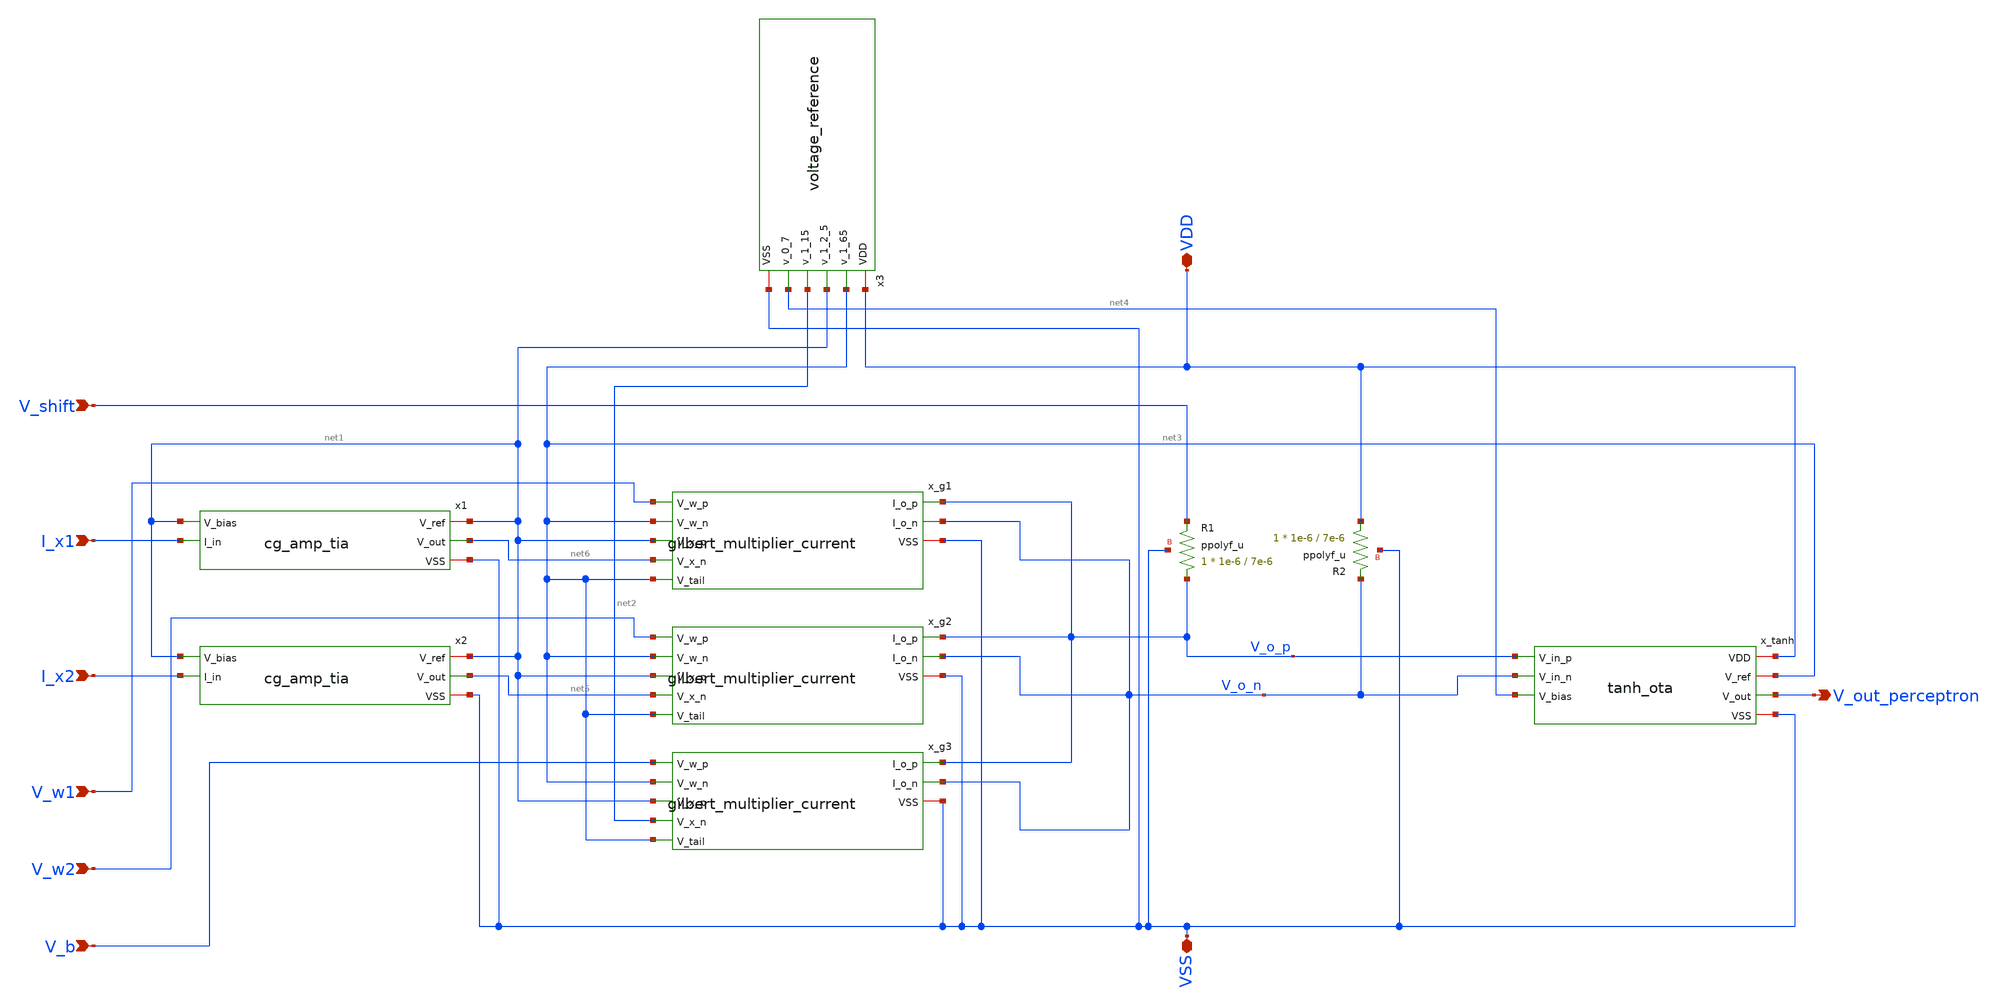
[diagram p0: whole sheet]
** sch_path: schematics/perceptron.sch
**.subckt perceptron VDD VSS I_x1 I_x2 V_w1 V_w2 V_b V_out_perceptron V_shift
*.iopin VDD
*.iopin VSS
*.ipin I_x1
*.ipin I_x2
*.ipin V_w1
*.ipin V_w2
*.ipin V_b
*.opin V_out_perceptron
*.ipin V_shift
x1 net1 net6 net1 I_x1 VSS cg_amp_tia
x2 net1 net5 net1 I_x2 VSS cg_amp_tia
x_g1 V_o_p V_o_n V_w1 net3 net1 net6 net3 VSS gilbert_multiplier_current
x_g2 V_o_p V_o_n V_w2 net3 net1 net5 net3 VSS gilbert_multiplier_current
x_g3 V_o_p V_o_n V_b net3 net1 net2 net3 VSS gilbert_multiplier_current
x_tanh VDD net3 V_out_perceptron V_o_p V_o_n net4 VSS tanh_ota
XR1 V_o_p V_shift VSS ppolyf_u r_width=1e-6 r_length=7e-6 m=1
XR2 VDD V_o_n VSS ppolyf_u r_width=1e-6 r_length=7e-6 m=1
x3 VDD net3 net1 net2 net4 VSS voltage_reference
**.ends

* expanding   symbol:  analog-perceptron-gf180mcu/schematics/cg_amp_tia.sym # of pins=5
** sym_path: schematics/cg_amp_tia.sym
** sch_path: schematics/cg_amp_tia.sch
.subckt cg_amp_tia V_ref V_out V_bias I_in VSS
*.iopin V_ref
*.iopin VSS
*.ipin I_in
*.ipin V_bias
*.opin V_out
XM1 V_out V_bias I_in VSS nfet_03v3 L=0.5u W=10u nf=1 ad='int((nf+1)/2) * W/nf * 0.18u' as='int((nf+2)/2) * W/nf * 0.18u'
+ pd='2*int((nf+1)/2) * (W/nf + 0.18u)' ps='2*int((nf+2)/2) * (W/nf + 0.18u)' nrd='0.18u / W' nrs='0.18u / W'
+ sa=0 sb=0 sd=0 m=1
XR1 V_out V_ref VSS ppolyf_u_1k r_width=1e-6 r_length=2.7e-6 m=1
.ends


* expanding   symbol:  analog-perceptron-gf180mcu/schematics/gilbert_multiplier_current.sym # of
*+ pins=8
** sym_path: schematics/gilbert_multiplier_current.sym
** sch_path: schematics/gilbert_multiplier_current.sch
.subckt gilbert_multiplier_current I_o_p I_o_n V_w_p V_w_n V_x_p V_x_n V_tail VSS
*.ipin V_x_p
*.ipin V_x_n
*.ipin V_tail
*.iopin VSS
*.ipin V_w_p
*.ipin V_w_n
*.opin I_o_n
*.opin I_o_p
XM1 net1 V_x_p net3 VSS nfet_03v3 L=0.5u W=10u nf=1 ad='int((nf+1)/2) * W/nf * 0.18u' as='int((nf+2)/2) * W/nf * 0.18u'
+ pd='2*int((nf+1)/2) * (W/nf + 0.18u)' ps='2*int((nf+2)/2) * (W/nf + 0.18u)' nrd='0.18u / W' nrs='0.18u / W'
+ sa=0 sb=0 sd=0 m=1
XM2 net2 V_x_n net4 VSS nfet_03v3 L=0.5u W=10u nf=1 ad='int((nf+1)/2) * W/nf * 0.18u' as='int((nf+2)/2) * W/nf * 0.18u'
+ pd='2*int((nf+1)/2) * (W/nf + 0.18u)' ps='2*int((nf+2)/2) * (W/nf + 0.18u)' nrd='0.18u / W' nrs='0.18u / W'
+ sa=0 sb=0 sd=0 m=1
XM3 I_o_n V_w_p net1 VSS nfet_03v3 L=0.5u W=10u nf=1 ad='int((nf+1)/2) * W/nf * 0.18u' as='int((nf+2)/2) * W/nf * 0.18u'
+ pd='2*int((nf+1)/2) * (W/nf + 0.18u)' ps='2*int((nf+2)/2) * (W/nf + 0.18u)' nrd='0.18u / W' nrs='0.18u / W'
+ sa=0 sb=0 sd=0 m=1
XM4 I_o_p V_w_n net1 VSS nfet_03v3 L=0.5u W=10u nf=1 ad='int((nf+1)/2) * W/nf * 0.18u' as='int((nf+2)/2) * W/nf * 0.18u'
+ pd='2*int((nf+1)/2) * (W/nf + 0.18u)' ps='2*int((nf+2)/2) * (W/nf + 0.18u)' nrd='0.18u / W' nrs='0.18u / W'
+ sa=0 sb=0 sd=0 m=1
XM5 I_o_n V_w_n net2 VSS nfet_03v3 L=0.5u W=10u nf=1 ad='int((nf+1)/2) * W/nf * 0.18u' as='int((nf+2)/2) * W/nf * 0.18u'
+ pd='2*int((nf+1)/2) * (W/nf + 0.18u)' ps='2*int((nf+2)/2) * (W/nf + 0.18u)' nrd='0.18u / W' nrs='0.18u / W'
+ sa=0 sb=0 sd=0 m=1
XM6 I_o_p V_w_p net2 VSS nfet_03v3 L=0.5u W=10u nf=1 ad='int((nf+1)/2) * W/nf * 0.18u' as='int((nf+2)/2) * W/nf * 0.18u'
+ pd='2*int((nf+1)/2) * (W/nf + 0.18u)' ps='2*int((nf+2)/2) * (W/nf + 0.18u)' nrd='0.18u / W' nrs='0.18u / W'
+ sa=0 sb=0 sd=0 m=1
XM7 net3 V_tail VSS VSS nfet_03v3 L=1u W=5u nf=1 ad='int((nf+1)/2) * W/nf * 0.18u' as='int((nf+2)/2) * W/nf * 0.18u'
+ pd='2*int((nf+1)/2) * (W/nf + 0.18u)' ps='2*int((nf+2)/2) * (W/nf + 0.18u)' nrd='0.18u / W' nrs='0.18u / W'
+ sa=0 sb=0 sd=0 m=1
XM8 net4 V_tail VSS VSS nfet_03v3 L=1u W=5u nf=1 ad='int((nf+1)/2) * W/nf * 0.18u' as='int((nf+2)/2) * W/nf * 0.18u'
+ pd='2*int((nf+1)/2) * (W/nf + 0.18u)' ps='2*int((nf+2)/2) * (W/nf + 0.18u)' nrd='0.18u / W' nrs='0.18u / W'
+ sa=0 sb=0 sd=0 m=1
XR1 net3 net4 VSS ppolyf_u_1k r_width=1e-6 r_length=15.4e-6 m=1
.ends


* expanding   symbol:  analog-perceptron-gf180mcu/schematics/tanh_ota.sym # of pins=7
** sym_path: schematics/tanh_ota.sym
** sch_path: schematics/tanh_ota.sch
.subckt tanh_ota VDD V_ref V_out V_in_p V_in_n V_bias VSS
*.iopin VDD
*.iopin VSS
*.ipin V_in_p
*.ipin V_in_n
*.ipin V_bias
*.opin V_out
*.iopin V_ref
XM1 net2 V_in_p net1 VSS nfet_03v3 L=0.5u W=10u nf=1 ad='int((nf+1)/2) * W/nf * 0.18u' as='int((nf+2)/2) * W/nf * 0.18u'
+ pd='2*int((nf+1)/2) * (W/nf + 0.18u)' ps='2*int((nf+2)/2) * (W/nf + 0.18u)' nrd='0.18u / W' nrs='0.18u / W'
+ sa=0 sb=0 sd=0 m=1
XM2 V_out V_in_n net1 VSS nfet_03v3 L=0.5u W=10u nf=1 ad='int((nf+1)/2) * W/nf * 0.18u' as='int((nf+2)/2) * W/nf * 0.18u'
+ pd='2*int((nf+1)/2) * (W/nf + 0.18u)' ps='2*int((nf+2)/2) * (W/nf + 0.18u)' nrd='0.18u / W' nrs='0.18u / W'
+ sa=0 sb=0 sd=0 m=1
XM3 net1 V_bias VSS VSS nfet_03v3 L=0.5u W=10u nf=1 ad='int((nf+1)/2) * W/nf * 0.18u' as='int((nf+2)/2) * W/nf * 0.18u'
+ pd='2*int((nf+1)/2) * (W/nf + 0.18u)' ps='2*int((nf+2)/2) * (W/nf + 0.18u)' nrd='0.18u / W' nrs='0.18u / W'
+ sa=0 sb=0 sd=0 m=1
XM4 net2 net2 VDD VDD pfet_03v3 L=0.5u W=20u nf=1 ad='int((nf+1)/2) * W/nf * 0.18u' as='int((nf+2)/2) * W/nf * 0.18u'
+ pd='2*int((nf+1)/2) * (W/nf + 0.18u)' ps='2*int((nf+2)/2) * (W/nf + 0.18u)' nrd='0.18u / W' nrs='0.18u / W'
+ sa=0 sb=0 sd=0 m=1
XM5 V_out net2 VDD VDD pfet_03v3 L=0.5u W=20u nf=1 ad='int((nf+1)/2) * W/nf * 0.18u' as='int((nf+2)/2) * W/nf * 0.18u'
+ pd='2*int((nf+1)/2) * (W/nf + 0.18u)' ps='2*int((nf+2)/2) * (W/nf + 0.18u)' nrd='0.18u / W' nrs='0.18u / W'
+ sa=0 sb=0 sd=0 m=1
XR1 V_out V_ref VSS ppolyf_u_1k r_width=1e-6 r_length=24.8e-6 m=1
.ends


* expanding   symbol:  analog-perceptron-gf180mcu/schematics/voltage_reference.sym # of pins=6
** sym_path: schematics/voltage_reference.sym
** sch_path: schematics/voltage_reference.sch
.subckt voltage_reference VDD v_1_65 v_1_2_5 v_1_15 v_0_7 VSS
*.iopin VDD
*.iopin VSS
*.opin v_1_65
*.opin v_1_2_5
*.opin v_1_15
*.opin v_0_7
XR1 v_1_65 VDD VSS ppolyf_u_1k r_width=1.5e-6 r_length=11.98e-6 m=24
XR2 v_1_2_5 v_1_65 VSS ppolyf_u_1k r_width=1.5e-6 r_length=2.78e-6 m=24
XR3 v_1_15 v_1_2_5 VSS ppolyf_u_1k r_width=1.5e-6 r_length=0.57e-6 m=24
XR4 v_0_7 v_1_15 VSS ppolyf_u_1k r_width=1.5e-6 r_length=3.15e-6 m=24
XR5 VSS v_0_7 VSS ppolyf_u_1k r_width=1.5e-6 r_length=4.99e-6 m=24
.ends

.end
